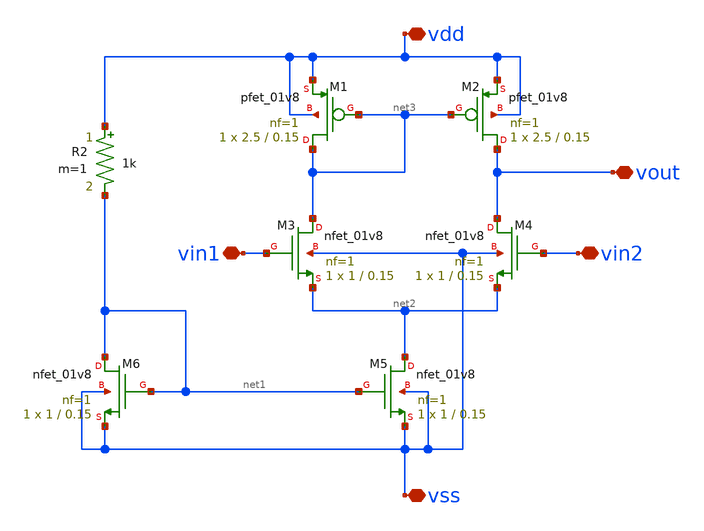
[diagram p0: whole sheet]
** sch_path: OPAMP/opamp.sch
**.subckt opamp vin2 vin1 vdd vss vout
*.iopin vin2
*.iopin vin1
*.iopin vdd
*.iopin vss
*.iopin vout
XM1 net3 net3 vdd vdd sky130_fd_pr__pfet_01v8 L=0.15 W=2.5 nf=1 ad='int((nf+1)/2) * W/nf * 0.29' as='int((nf+2)/2) * W/nf * 0.29'
+ pd='2*int((nf+1)/2) * (W/nf + 0.29)' ps='2*int((nf+2)/2) * (W/nf + 0.29)' nrd='0.29 / W' nrs='0.29 / W'
+ sa=0 sb=0 sd=0 mult=1 m=1
XM2 vout net3 vdd vdd sky130_fd_pr__pfet_01v8 L=0.15 W=2.5 nf=1 ad='int((nf+1)/2) * W/nf * 0.29' as='int((nf+2)/2) * W/nf * 0.29'
+ pd='2*int((nf+1)/2) * (W/nf + 0.29)' ps='2*int((nf+2)/2) * (W/nf + 0.29)' nrd='0.29 / W' nrs='0.29 / W'
+ sa=0 sb=0 sd=0 mult=1 m=1
XM3 net3 vin1 net2 vss sky130_fd_pr__nfet_01v8 L=0.15 W=1 nf=1 ad='int((nf+1)/2) * W/nf * 0.29' as='int((nf+2)/2) * W/nf * 0.29'
+ pd='2*int((nf+1)/2) * (W/nf + 0.29)' ps='2*int((nf+2)/2) * (W/nf + 0.29)' nrd='0.29 / W' nrs='0.29 / W'
+ sa=0 sb=0 sd=0 mult=1 m=1
XM4 vout vin2 net2 vss sky130_fd_pr__nfet_01v8 L=0.15 W=1 nf=1 ad='int((nf+1)/2) * W/nf * 0.29' as='int((nf+2)/2) * W/nf * 0.29'
+ pd='2*int((nf+1)/2) * (W/nf + 0.29)' ps='2*int((nf+2)/2) * (W/nf + 0.29)' nrd='0.29 / W' nrs='0.29 / W'
+ sa=0 sb=0 sd=0 mult=1 m=1
XM5 net2 net1 vss vss sky130_fd_pr__nfet_01v8 L=0.15 W=1 nf=1 ad='int((nf+1)/2) * W/nf * 0.29' as='int((nf+2)/2) * W/nf * 0.29'
+ pd='2*int((nf+1)/2) * (W/nf + 0.29)' ps='2*int((nf+2)/2) * (W/nf + 0.29)' nrd='0.29 / W' nrs='0.29 / W'
+ sa=0 sb=0 sd=0 mult=1 m=1
XM6 net1 net1 vss vss sky130_fd_pr__nfet_01v8 L=0.15 W=1 nf=1 ad='int((nf+1)/2) * W/nf * 0.29' as='int((nf+2)/2) * W/nf * 0.29'
+ pd='2*int((nf+1)/2) * (W/nf + 0.29)' ps='2*int((nf+2)/2) * (W/nf + 0.29)' nrd='0.29 / W' nrs='0.29 / W'
+ sa=0 sb=0 sd=0 mult=1 m=1
R2 vdd net1 1k m=1
**.ends
.end
